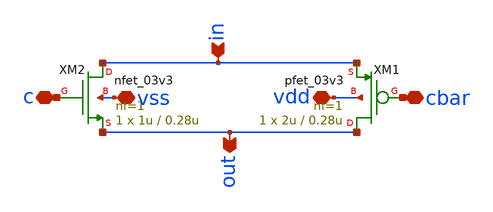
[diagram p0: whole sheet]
** sch_path: schematics/PC/TG/TG.sch
**.subckt TG in out vss vdd c cbar
*.ipin in
*.opin out
*.iopin vss
*.iopin vdd
*.iopin c
*.iopin cbar
XM1 out cbar in vdd pfet_03v3 L=0.28u W=2u nf=1 ad='int((nf+1)/2) * W/nf * 0.18u' as='int((nf+2)/2) * W/nf * 0.18u'
+ pd='2*int((nf+1)/2) * (W/nf + 0.18u)' ps='2*int((nf+2)/2) * (W/nf + 0.18u)' nrd='0.18u / W' nrs='0.18u / W'
+ sa=0 sb=0 sd=0 m=1
XM2 in c out vss nfet_03v3 L=0.28u W=1u nf=1 ad='int((nf+1)/2) * W/nf * 0.18u' as='int((nf+2)/2) * W/nf * 0.18u'
+ pd='2*int((nf+1)/2) * (W/nf + 0.18u)' ps='2*int((nf+2)/2) * (W/nf + 0.18u)' nrd='0.18u / W' nrs='0.18u / W'
+ sa=0 sb=0 sd=0 m=1
**.ends
.end
